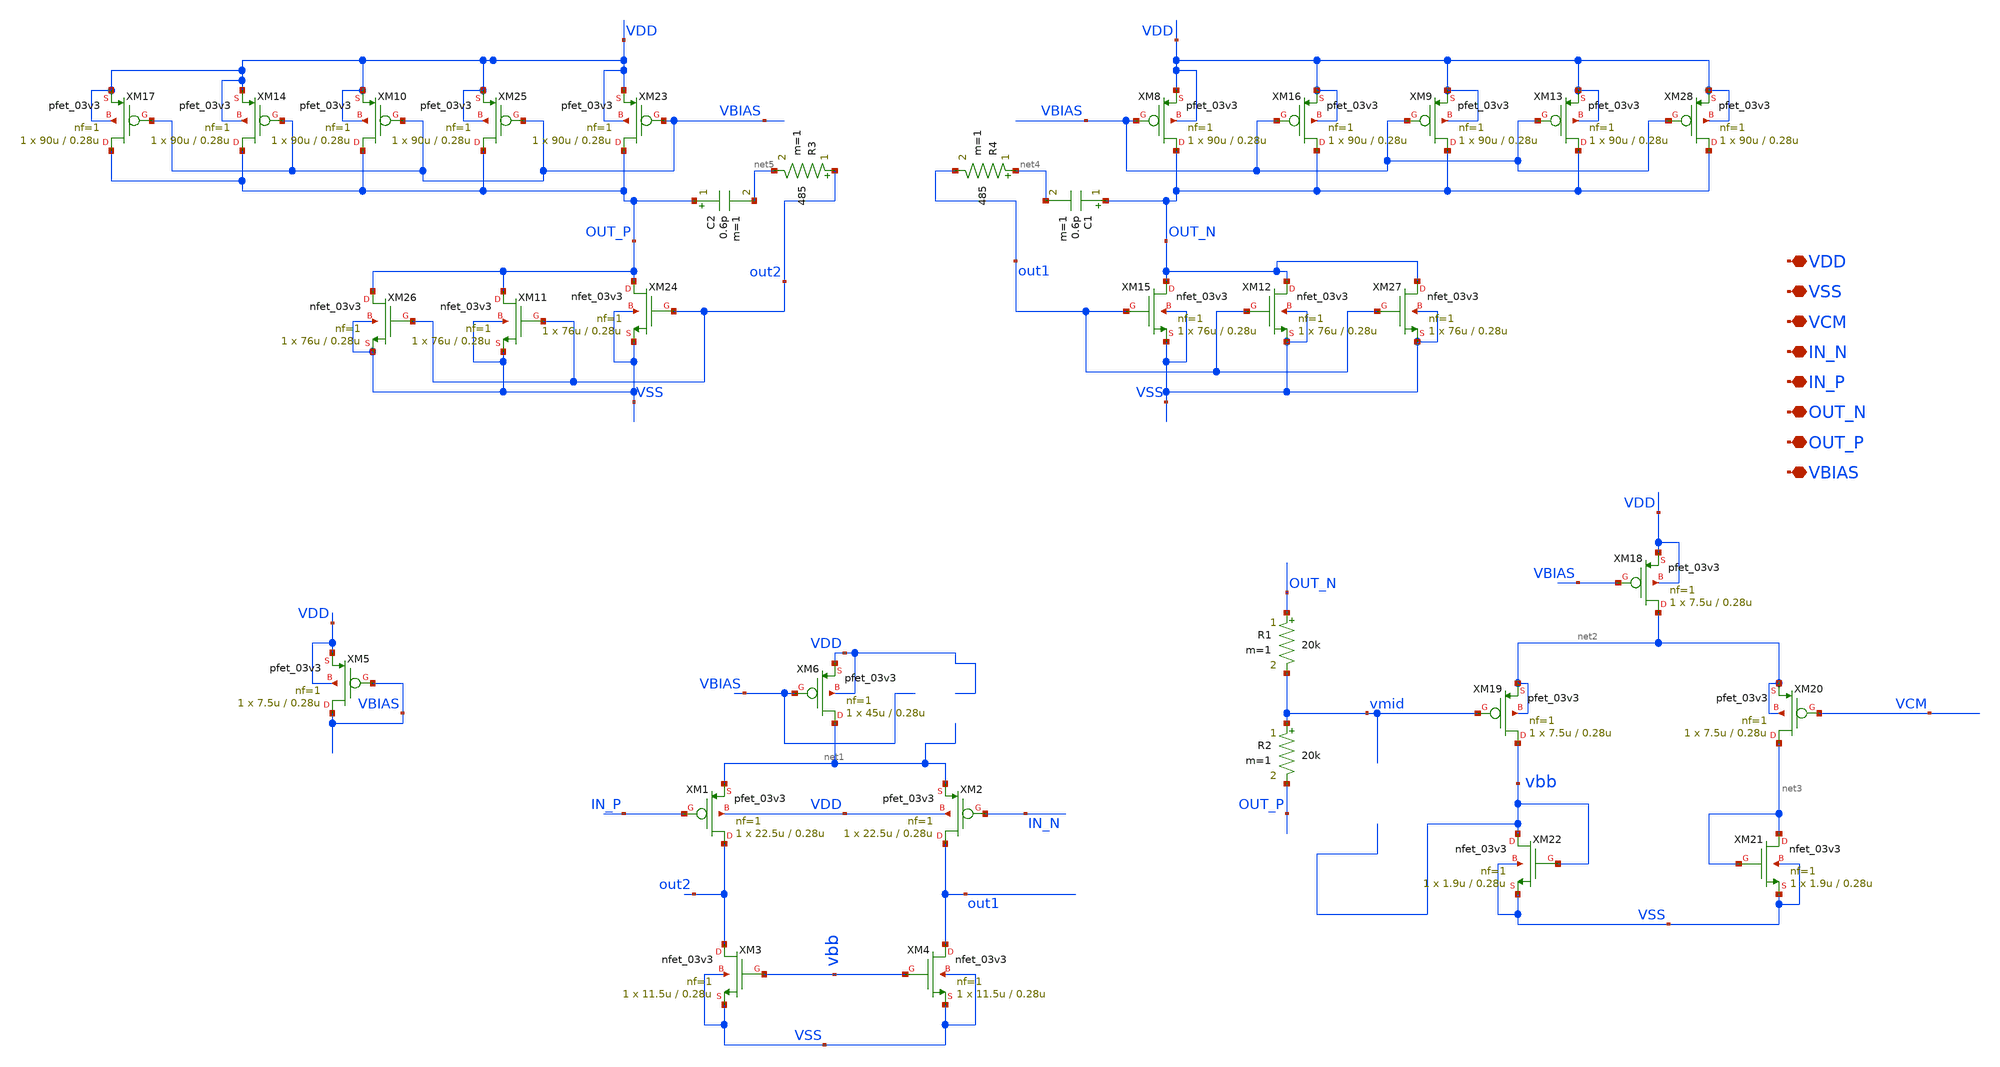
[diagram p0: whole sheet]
** sch_path: SCOP_INPUT_AND_MUX_PAKISTAN_03/Xschem/Folded_single/Two_Stage_OTA.sch
**.subckt Two_Stage_OTA VDD VSS VCM IN_N IN_P OUT_N OUT_P VBIAS
*.iopin VDD
*.iopin VSS
*.iopin VCM
*.iopin IN_N
*.iopin IN_P
*.iopin OUT_N
*.iopin OUT_P
*.iopin VBIAS
XM1 out2 IN_P net1 VDD pfet_03v3 L=0.28u W=22.5u nf=1 ad='int((nf+1)/2) * W/nf * 0.18u' as='int((nf+2)/2) * W/nf * 0.18u'
+ pd='2*int((nf+1)/2) * (W/nf + 0.18u)' ps='2*int((nf+2)/2) * (W/nf + 0.18u)' nrd='0.18u / W' nrs='0.18u / W'
+ sa=0 sb=0 sd=0 m=1
XM2 out1 IN_N net1 VDD pfet_03v3 L=0.28u W=22.5u nf=1 ad='int((nf+1)/2) * W/nf * 0.18u' as='int((nf+2)/2) * W/nf * 0.18u'
+ pd='2*int((nf+1)/2) * (W/nf + 0.18u)' ps='2*int((nf+2)/2) * (W/nf + 0.18u)' nrd='0.18u / W' nrs='0.18u / W'
+ sa=0 sb=0 sd=0 m=1
XM3 out2 vbb VSS VSS nfet_03v3 L=0.28u W=11.5u nf=1 ad='int((nf+1)/2) * W/nf * 0.18u' as='int((nf+2)/2) * W/nf * 0.18u'
+ pd='2*int((nf+1)/2) * (W/nf + 0.18u)' ps='2*int((nf+2)/2) * (W/nf + 0.18u)' nrd='0.18u / W' nrs='0.18u / W'
+ sa=0 sb=0 sd=0 m=1
XM4 out1 vbb VSS VSS nfet_03v3 L=0.28u W=11.5u nf=1 ad='int((nf+1)/2) * W/nf * 0.18u' as='int((nf+2)/2) * W/nf * 0.18u'
+ pd='2*int((nf+1)/2) * (W/nf + 0.18u)' ps='2*int((nf+2)/2) * (W/nf + 0.18u)' nrd='0.18u / W' nrs='0.18u / W'
+ sa=0 sb=0 sd=0 m=1
XM5 VBIAS VBIAS VDD VDD pfet_03v3 L=0.28u W=7.5u nf=1 ad='int((nf+1)/2) * W/nf * 0.18u' as='int((nf+2)/2) * W/nf * 0.18u'
+ pd='2*int((nf+1)/2) * (W/nf + 0.18u)' ps='2*int((nf+2)/2) * (W/nf + 0.18u)' nrd='0.18u / W' nrs='0.18u / W'
+ sa=0 sb=0 sd=0 m=1
XM18 net2 VBIAS VDD VDD pfet_03v3 L=0.28u W=7.5u nf=1 ad='int((nf+1)/2) * W/nf * 0.18u' as='int((nf+2)/2) * W/nf * 0.18u'
+ pd='2*int((nf+1)/2) * (W/nf + 0.18u)' ps='2*int((nf+2)/2) * (W/nf + 0.18u)' nrd='0.18u / W' nrs='0.18u / W'
+ sa=0 sb=0 sd=0 m=1
XM19 vbb vmid net2 net2 pfet_03v3 L=0.28u W=7.5u nf=1 ad='int((nf+1)/2) * W/nf * 0.18u' as='int((nf+2)/2) * W/nf * 0.18u'
+ pd='2*int((nf+1)/2) * (W/nf + 0.18u)' ps='2*int((nf+2)/2) * (W/nf + 0.18u)' nrd='0.18u / W' nrs='0.18u / W'
+ sa=0 sb=0 sd=0 m=1
XM20 net3 VCM net2 net2 pfet_03v3 L=0.28u W=7.5u nf=1 ad='int((nf+1)/2) * W/nf * 0.18u' as='int((nf+2)/2) * W/nf * 0.18u'
+ pd='2*int((nf+1)/2) * (W/nf + 0.18u)' ps='2*int((nf+2)/2) * (W/nf + 0.18u)' nrd='0.18u / W' nrs='0.18u / W'
+ sa=0 sb=0 sd=0 m=1
XM21 net3 net3 VSS VSS nfet_03v3 L=0.28u W=1.9u nf=1 ad='int((nf+1)/2) * W/nf * 0.18u' as='int((nf+2)/2) * W/nf * 0.18u'
+ pd='2*int((nf+1)/2) * (W/nf + 0.18u)' ps='2*int((nf+2)/2) * (W/nf + 0.18u)' nrd='0.18u / W' nrs='0.18u / W'
+ sa=0 sb=0 sd=0 m=1
XM22 vbb vbb VSS VSS nfet_03v3 L=0.28u W=1.9u nf=1 ad='int((nf+1)/2) * W/nf * 0.18u' as='int((nf+2)/2) * W/nf * 0.18u'
+ pd='2*int((nf+1)/2) * (W/nf + 0.18u)' ps='2*int((nf+2)/2) * (W/nf + 0.18u)' nrd='0.18u / W' nrs='0.18u / W'
+ sa=0 sb=0 sd=0 m=1
R1 OUT_N vmid 20k m=1
R2 vmid OUT_P 20k m=1
XM6 net1 VBIAS VDD VDD pfet_03v3 L=0.28u W=45u nf=1 ad='int((nf+1)/2) * W/nf * 0.18u' as='int((nf+2)/2) * W/nf * 0.18u'
+ pd='2*int((nf+1)/2) * (W/nf + 0.18u)' ps='2*int((nf+2)/2) * (W/nf + 0.18u)' nrd='0.18u / W' nrs='0.18u / W'
+ sa=0 sb=0 sd=0 m=1
XM8 OUT_N VBIAS VDD VDD pfet_03v3 L=0.28u W=90u nf=1 ad='int((nf+1)/2) * W/nf * 0.18u' as='int((nf+2)/2) * W/nf * 0.18u'
+ pd='2*int((nf+1)/2) * (W/nf + 0.18u)' ps='2*int((nf+2)/2) * (W/nf + 0.18u)' nrd='0.18u / W' nrs='0.18u / W'
+ sa=0 sb=0 sd=0 m=1
XM15 OUT_N out1 VSS VSS nfet_03v3 L=0.28u W=76u nf=1 ad='int((nf+1)/2) * W/nf * 0.18u' as='int((nf+2)/2) * W/nf * 0.18u'
+ pd='2*int((nf+1)/2) * (W/nf + 0.18u)' ps='2*int((nf+2)/2) * (W/nf + 0.18u)' nrd='0.18u / W' nrs='0.18u / W'
+ sa=0 sb=0 sd=0 m=1
C1 OUT_N net4 0.6p m=1
XM16 OUT_N VBIAS VDD VDD pfet_03v3 L=0.28u W=90u nf=1 ad='int((nf+1)/2) * W/nf * 0.18u' as='int((nf+2)/2) * W/nf * 0.18u'
+ pd='2*int((nf+1)/2) * (W/nf + 0.18u)' ps='2*int((nf+2)/2) * (W/nf + 0.18u)' nrd='0.18u / W' nrs='0.18u / W'
+ sa=0 sb=0 sd=0 m=1
XM23 OUT_P VBIAS VDD VDD pfet_03v3 L=0.28u W=90u nf=1 ad='int((nf+1)/2) * W/nf * 0.18u' as='int((nf+2)/2) * W/nf * 0.18u'
+ pd='2*int((nf+1)/2) * (W/nf + 0.18u)' ps='2*int((nf+2)/2) * (W/nf + 0.18u)' nrd='0.18u / W' nrs='0.18u / W'
+ sa=0 sb=0 sd=0 m=1
XM24 OUT_P out2 VSS VSS nfet_03v3 L=0.28u W=76u nf=1 ad='int((nf+1)/2) * W/nf * 0.18u' as='int((nf+2)/2) * W/nf * 0.18u'
+ pd='2*int((nf+1)/2) * (W/nf + 0.18u)' ps='2*int((nf+2)/2) * (W/nf + 0.18u)' nrd='0.18u / W' nrs='0.18u / W'
+ sa=0 sb=0 sd=0 m=1
C2 OUT_P net5 0.6p m=1
XM25 OUT_P VBIAS VDD VDD pfet_03v3 L=0.28u W=90u nf=1 ad='int((nf+1)/2) * W/nf * 0.18u' as='int((nf+2)/2) * W/nf * 0.18u'
+ pd='2*int((nf+1)/2) * (W/nf + 0.18u)' ps='2*int((nf+2)/2) * (W/nf + 0.18u)' nrd='0.18u / W' nrs='0.18u / W'
+ sa=0 sb=0 sd=0 m=1
R3 out2 net5 485 m=1
R4 net4 out1 485 m=1
XM9 OUT_N VBIAS VDD VDD pfet_03v3 L=0.28u W=90u nf=1 ad='int((nf+1)/2) * W/nf * 0.18u' as='int((nf+2)/2) * W/nf * 0.18u'
+ pd='2*int((nf+1)/2) * (W/nf + 0.18u)' ps='2*int((nf+2)/2) * (W/nf + 0.18u)' nrd='0.18u / W' nrs='0.18u / W'
+ sa=0 sb=0 sd=0 m=1
XM10 OUT_P VBIAS VDD VDD pfet_03v3 L=0.28u W=90u nf=1 ad='int((nf+1)/2) * W/nf * 0.18u' as='int((nf+2)/2) * W/nf * 0.18u'
+ pd='2*int((nf+1)/2) * (W/nf + 0.18u)' ps='2*int((nf+2)/2) * (W/nf + 0.18u)' nrd='0.18u / W' nrs='0.18u / W'
+ sa=0 sb=0 sd=0 m=1
XM11 OUT_P out2 VSS VSS nfet_03v3 L=0.28u W=76u nf=1 ad='int((nf+1)/2) * W/nf * 0.18u' as='int((nf+2)/2) * W/nf * 0.18u'
+ pd='2*int((nf+1)/2) * (W/nf + 0.18u)' ps='2*int((nf+2)/2) * (W/nf + 0.18u)' nrd='0.18u / W' nrs='0.18u / W'
+ sa=0 sb=0 sd=0 m=1
XM12 OUT_N out1 VSS VSS nfet_03v3 L=0.28u W=76u nf=1 ad='int((nf+1)/2) * W/nf * 0.18u' as='int((nf+2)/2) * W/nf * 0.18u'
+ pd='2*int((nf+1)/2) * (W/nf + 0.18u)' ps='2*int((nf+2)/2) * (W/nf + 0.18u)' nrd='0.18u / W' nrs='0.18u / W'
+ sa=0 sb=0 sd=0 m=1
XM13 OUT_N VBIAS VDD VDD pfet_03v3 L=0.28u W=90u nf=1 ad='int((nf+1)/2) * W/nf * 0.18u' as='int((nf+2)/2) * W/nf * 0.18u'
+ pd='2*int((nf+1)/2) * (W/nf + 0.18u)' ps='2*int((nf+2)/2) * (W/nf + 0.18u)' nrd='0.18u / W' nrs='0.18u / W'
+ sa=0 sb=0 sd=0 m=1
XM14 OUT_P VBIAS VDD VDD pfet_03v3 L=0.28u W=90u nf=1 ad='int((nf+1)/2) * W/nf * 0.18u' as='int((nf+2)/2) * W/nf * 0.18u'
+ pd='2*int((nf+1)/2) * (W/nf + 0.18u)' ps='2*int((nf+2)/2) * (W/nf + 0.18u)' nrd='0.18u / W' nrs='0.18u / W'
+ sa=0 sb=0 sd=0 m=1
XM17 OUT_P VBIAS VDD VDD pfet_03v3 L=0.28u W=90u nf=1 ad='int((nf+1)/2) * W/nf * 0.18u' as='int((nf+2)/2) * W/nf * 0.18u'
+ pd='2*int((nf+1)/2) * (W/nf + 0.18u)' ps='2*int((nf+2)/2) * (W/nf + 0.18u)' nrd='0.18u / W' nrs='0.18u / W'
+ sa=0 sb=0 sd=0 m=1
XM26 OUT_P out2 VSS VSS nfet_03v3 L=0.28u W=76u nf=1 ad='int((nf+1)/2) * W/nf * 0.18u' as='int((nf+2)/2) * W/nf * 0.18u'
+ pd='2*int((nf+1)/2) * (W/nf + 0.18u)' ps='2*int((nf+2)/2) * (W/nf + 0.18u)' nrd='0.18u / W' nrs='0.18u / W'
+ sa=0 sb=0 sd=0 m=1
XM27 OUT_N out1 VSS VSS nfet_03v3 L=0.28u W=76u nf=1 ad='int((nf+1)/2) * W/nf * 0.18u' as='int((nf+2)/2) * W/nf * 0.18u'
+ pd='2*int((nf+1)/2) * (W/nf + 0.18u)' ps='2*int((nf+2)/2) * (W/nf + 0.18u)' nrd='0.18u / W' nrs='0.18u / W'
+ sa=0 sb=0 sd=0 m=1
XM28 OUT_N VBIAS VDD VDD pfet_03v3 L=0.28u W=90u nf=1 ad='int((nf+1)/2) * W/nf * 0.18u' as='int((nf+2)/2) * W/nf * 0.18u'
+ pd='2*int((nf+1)/2) * (W/nf + 0.18u)' ps='2*int((nf+2)/2) * (W/nf + 0.18u)' nrd='0.18u / W' nrs='0.18u / W'
+ sa=0 sb=0 sd=0 m=1
**.ends
.end
